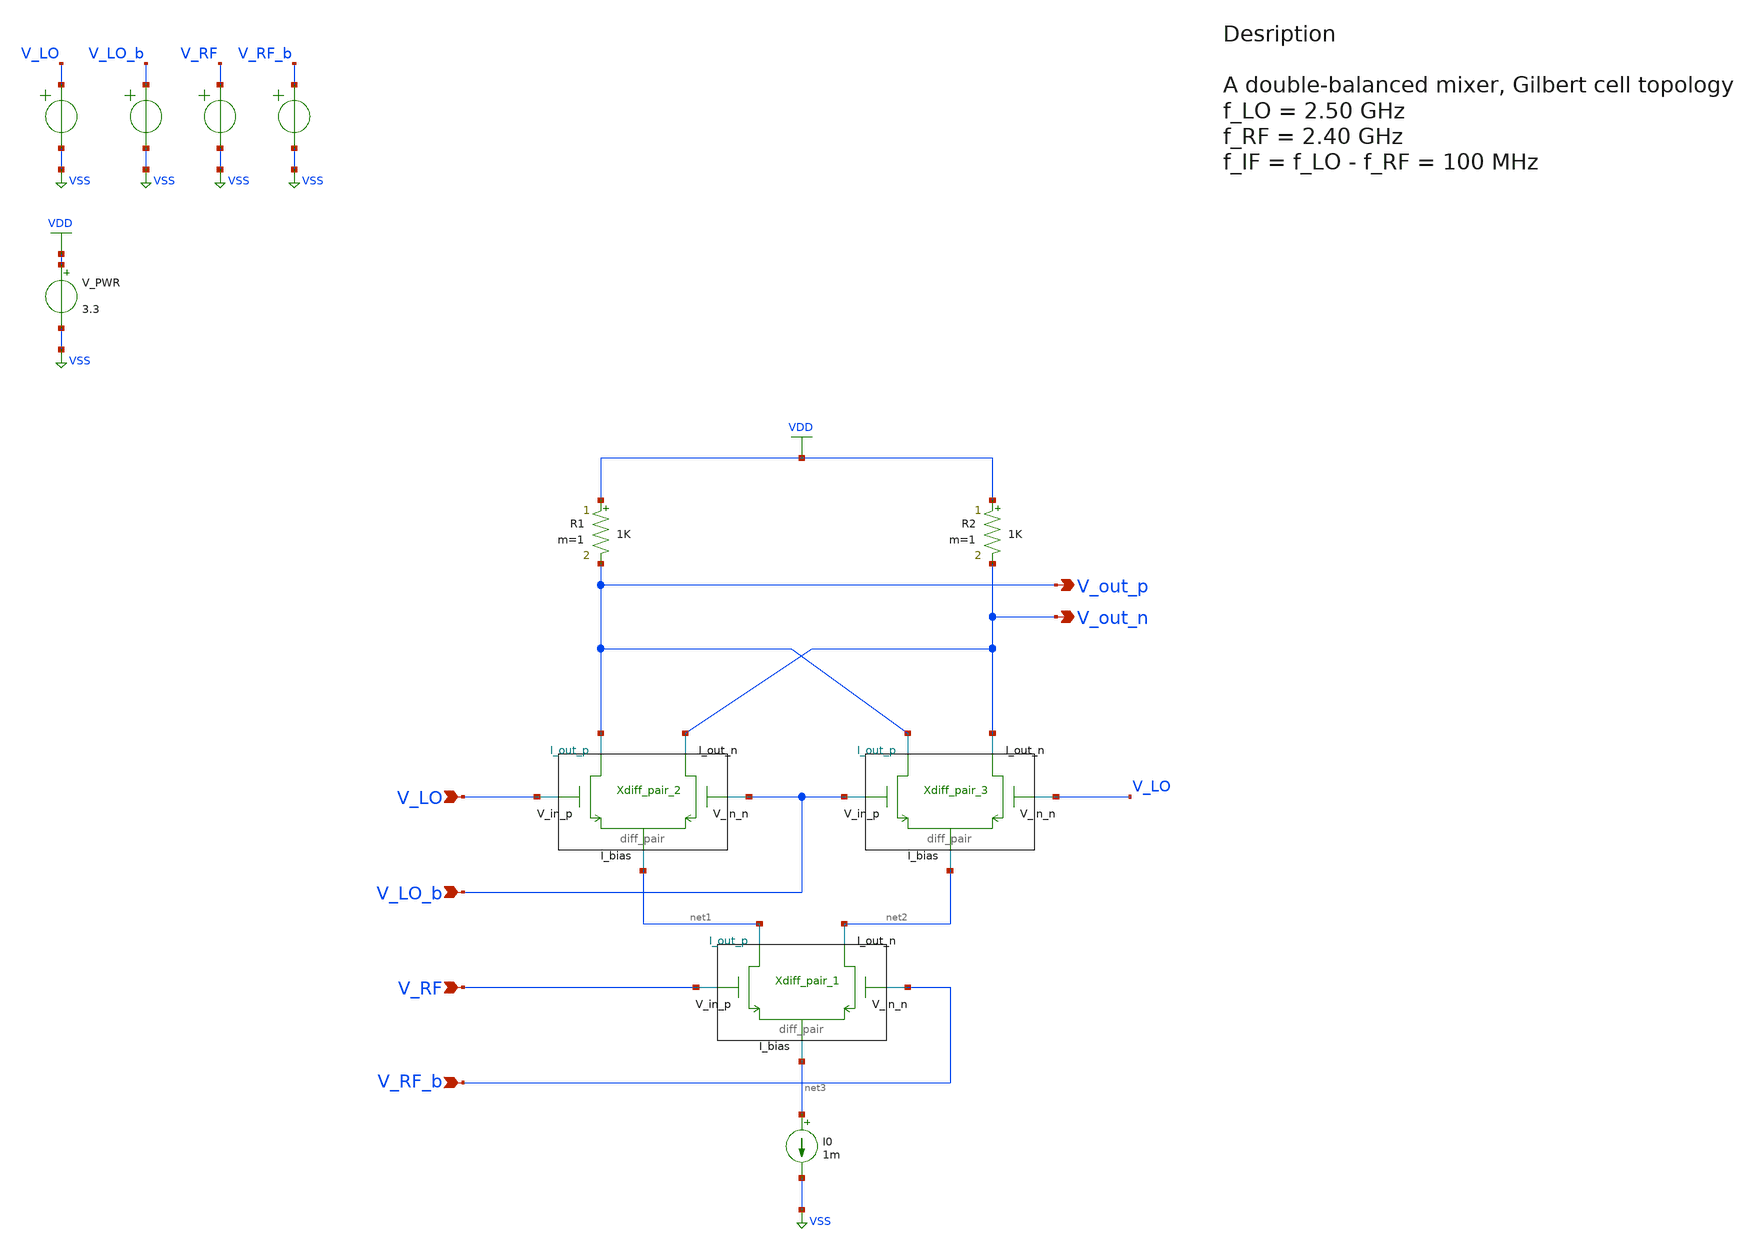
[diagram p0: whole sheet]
** sch_path: src/design_xsch/Gilbert_cell.sch
**.subckt Gilbert_cell V_LO V_LO_b V_RF V_RF_b V_out_p V_out_n
*.ipin V_LO
*.ipin V_LO_b
*.ipin V_RF
*.ipin V_RF_b
*.opin V_out_p
*.opin V_out_n
I0 net3 VSS 1m
E1 V_LO VSS VOL=' '1.5 + sin(time * 2.5 * 1e9)' '
E2 V_LO_b VSS VOL=' '1.5 - sin(time * 2.5 * 1e9)' '
E4 V_RF VSS VOL=' '1.5 + sin(time * 2.40 * 1e9)' '
E6 V_RF_b VSS VOL=' '1.5 - sin(time * 2.40 * 1e9)' '
Xdiff_pair_1 net2 net1 V_RF V_RF_b net3 VSS diff_pair W_neg=0.22u L_neg=0.28u W_pos=2u L_pos=0.28u
+ m=1
Xdiff_pair_2 V_out_n V_out_p V_LO V_LO_b net1 VSS diff_pair W_neg=0.22u L_neg=0.28u W_pos=0.22u
+ L_pos=0.28u m=1
Xdiff_pair_3 V_out_n V_out_p V_LO_b V_LO net2 VSS diff_pair W_neg=0.22u L_neg=0.28u W_pos=0.22u
+ L_pos=0.28u m=1
R1 VDD V_out_p 1K m=1
R2 VDD V_out_n 1K m=1
V_PWR VDD VSS 3.3
.save i(v_pwr)
**** begin user architecture code

.include $::180MCU_MODELS/design.ngspice
.lib $::180MCU_MODELS/sm141064.ngspice typical



.control

    save all

    * Define frequencies
    let f_lo = 2.5e9
    let f_rf = 2.4e9
    let f_if = 100e6

    * operating point
    op
    print all

    write Gilbert_cell.raw
    set appendwrite

    * Transient analysis to observe mixing operation
    tran 1p 50n

    * Calculate differential output for conversion gain measurement
    let v_out_diff = v(v_out_p) - v(v_out_n)
    let v_rf_diff = v(v_rf) - v(v_rf_b)

    * Extract IF component at 100MHz using FFT
    linearize v_out_diff v_rf_diff
    let time_step = 1e-12
    let sample_freq = 1/time_step
    let npts = length(v_out_diff)
    let freq_res = sample_freq/npts

    fft v_out_diff v_rf_diff

    * Find frequency bins
    let if_bin = floor(100e6/freq_res)
    let rf_bin = floor(2.4e9/freq_res)

    * Measure conversion gain (power gain from RF to IF)
    let rf_mag = abs(v_rf_diff[rf_bin])
    let if_mag = abs(v_out_diff[if_bin])
    let conversion_gain_db = 20*log10(if_mag/rf_mag)
    print conversion_gain_db

    write Gilbert_cell.raw

    * Two-tone test for IIP2 and IIP3 measurement
    * Reset sources for two-tone test
    alter @E4[VOL] = '1.5 + 0.05*sin(2*pi*2.39e9*time) + 0.05*sin(2*pi*2.41e9*time)'
    alter @E6[VOL] = '1.5 - 0.05*sin(2*pi*2.39e9*time) - 0.05*sin(2*pi*2.41e9*time)'

    tran 1p 100n

    * Calculate differential output for two-tone analysis
    let v_out_diff_2tone = v(v_out_p) - v(v_out_n)

    * Linearize and perform FFT for intermodulation analysis
    linearize v_out_diff_2tone
    let time_step = 1e-12
    let sample_freq = 1/time_step
    let npts = length(v_out_diff_2tone)
    let freq_res = sample_freq/npts

    fft v_out_diff_2tone
    let freq_axis = vector(npts)
    let freq_axis = freq_res * vector(npts)

    * Find frequency bins for measurements
    let if_bin = floor(100e6/freq_res)
    let im2_bin = floor(20e6/freq_res)
    let im3_low_bin = floor(80e6/freq_res)  ; 2*2.39-2.41 = 2.37 -> 100M - 20M = 80M at IF
    let im3_high_bin = floor(120e6/freq_res) ; 2*2.41-2.39 = 2.43 -> 100M + 20M = 120M at IF

    * Extract magnitudes at specific frequencies
    let fund_mag = abs(v_out_diff_2tone[if_bin])
    let im2_mag = abs(v_out_diff_2tone[im2_bin])
    let im3_mag = maximum(abs(v_out_diff_2tone[im3_low_bin]), abs(v_out_diff_2tone[im3_high_bin]))

    * Calculate IIP2 and IIP3 (simplified calculation)
    let input_power_dbm = 10*log10(0.05*0.05/50e-3) + 30  ; Input power in dBm (50 ohm)
    let iip2_dbm = input_power_dbm + (20*log10(fund_mag) - 20*log10(im2_mag))/2
    let iip3_dbm = input_power_dbm + (20*log10(fund_mag) - 20*log10(im3_mag))*2/3

    print iip2_dbm iip3_dbm

    write Gilbert_cell.raw

    * Noise analysis for Noise Figure calculation
    * Reset to single tone for noise analysis
    alter @E4[VOL] = '1.5 + 0.001*sin(2*pi*2.4e9*time)'  ; Small signal for noise
    alter @E6[VOL] = '1.5 - 0.001*sin(2*pi*2.4e9*time)'

    noise v(v_out_p,v_out_n) E4 dec 10 1e6 1e9

    * Calculate Single Sideband Noise Figure
    * NF_SSB = NF_DSB + 3dB (for double sideband to single sideband conversion)
    setplot noise1
    let nf_dsb_db = 10*log10(onoise_total^2/inoise_total^2)
    let nf_ssb_db = nf_dsb_db + 3
    print nf_ssb_db

    * Summary of measurements
    echo
    echo *** GILBERT CELL MIXER PERFORMANCE SUMMARY ***
    echo Conversion Gain: $&conversion_gain_db dB
    echo IIP2: $&iip2_dbm dBm
    echo IIP3: $&iip3_dbm dBm
    echo Single Sideband Noise Figure: $&nf_ssb_db dB
    echo

    write Gilbert_cell.raw
.endc


**** end user architecture code
**.ends

* expanding   symbol:  /home/vasil/Downloads/SSCS_PICO_2025/src/design_xsch/diff_pair.sym # of
*+ pins=5
** sym_path: src/design_xsch/diff_pair.sym
** sch_path: src/design_xsch/diff_pair.sch
.subckt diff_pair I_out_n I_out_p V_in_p V_in_n I_bias VSSPIN  mult=1  W_neg=0.22u L_neg=0.28u
+ W_pos=0.22u L_pos=0.28u
*.ipin V_in_p
*.ipin V_in_n
*.iopin I_out_p
*.iopin I_out_n
*.iopin I_bias
XM1 I_out_p V_in_p I_bias VSS nfet_03v3 L=L_pos W=W_pos nf=1 ad='int((nf+1)/2) * W/nf * 0.18u' as='int((nf+2)/2) * W/nf * 0.18u'
+ pd='2*int((nf+1)/2) * (W/nf + 0.18u)' ps='2*int((nf+2)/2) * (W/nf + 0.18u)' nrd='0.18u / W' nrs='0.18u / W'
+ sa=0 sb=0 sd=0 m=mult
XM2 I_out_n V_in_n I_bias VSS nfet_03v3 L=L_neg W=W_neg nf=1 ad='int((nf+1)/2) * W/nf * 0.18u' as='int((nf+2)/2) * W/nf * 0.18u'
+ pd='2*int((nf+1)/2) * (W/nf + 0.18u)' ps='2*int((nf+2)/2) * (W/nf + 0.18u)' nrd='0.18u / W' nrs='0.18u / W'
+ sa=0 sb=0 sd=0 m=mult
.ends

.GLOBAL VSS
.GLOBAL VDD
.end
